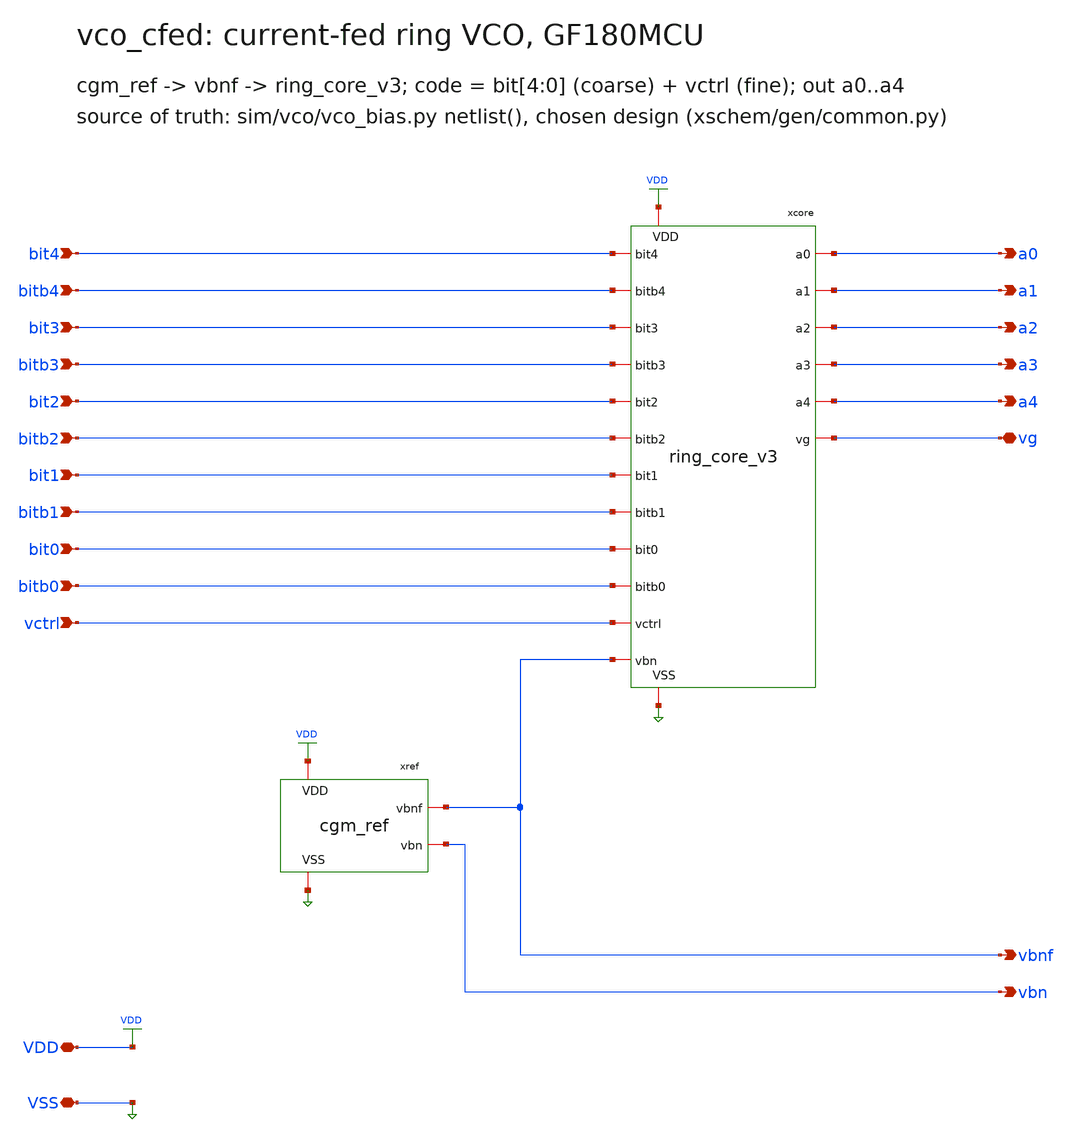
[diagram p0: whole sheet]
** sch_path: xschem/vco_cfed.sch
**.subckt vco_cfed VDD VSS vctrl bit0 bit1 bit2 bit3 bit4 bitb0 bitb1 bitb2 bitb3 bitb4 a0 a1 a2 a3
*+ a4 vg vbn vbnf
*.iopin VDD
*.iopin VSS
*.ipin vctrl
*.ipin bit0
*.ipin bit1
*.ipin bit2
*.ipin bit3
*.ipin bit4
*.ipin bitb0
*.ipin bitb1
*.ipin bitb2
*.ipin bitb3
*.ipin bitb4
*.opin a0
*.opin a1
*.opin a2
*.opin a3
*.opin a4
*.iopin vg
*.opin vbn
*.opin vbnf
xcore VDD VSS vbnf vctrl bit0 bit1 bit2 bit3 bit4 bitb0 bitb1 bitb2 bitb3 bitb4 vg a0 a1 a2 a3 a4
+ ring_core_v3
xref VDD VSS vbn vbnf cgm_ref
**.ends

* expanding   symbol:  ring_core_v3.sym # of pins=20
** sym_path: xschem/ring_core_v3.sym
** sch_path: xschem/ring_core_v3.sch
.subckt ring_core_v3 VDD VSS vbn vctrl bit0 bit1 bit2 bit3 bit4 bitb0 bitb1 bitb2 bitb3 bitb4 vg a0
+ a1 a2 a3 a4
*.iopin VDD
*.iopin VSS
*.ipin vbn
*.ipin vctrl
*.ipin bit0
*.ipin bit1
*.ipin bit2
*.ipin bit3
*.ipin bit4
*.ipin bitb0
*.ipin bitb1
*.ipin bitb2
*.ipin bitb3
*.ipin bitb4
*.iopin vg
*.opin a0
*.opin a1
*.opin a2
*.opin a3
*.opin a4
xdac vg vbn vctrl bit0 bit1 bit2 bit3 bit4 bitb0 bitb1 bitb2 bitb3 bitb4 VDD VSS cfed_dac
xring VDD vg VSS a0 a1 a2 a3 a4 cfed_ring
XDC VSS vg VSS VSS nfet_03v3 L=4.0u W=30.71u nf=1 ad=0 as=0 pd=0 ps=0 nrd=0 nrs=0 sa=0 sb=0 sd=0 m=6
.ends


* expanding   symbol:  cgm_ref.sym # of pins=4
** sym_path: xschem/cgm_ref.sym
** sch_path: xschem/cgm_ref.sch
.subckt cgm_ref VDD VSS vbn vbnf
*.iopin VDD
*.iopin VSS
*.opin vbn
*.opin vbnf
XMP2 net1 net1 VDD VDD pfet_03v3 L=14.0u W=56.0u nf=1 ad=28.0p as=28.0p pd=113.0u ps=113.0u nrd=0
+ nrs=0 sa=0 sb=0 sd=0 m=1
XMP1 vbn net1 VDD VDD pfet_03v3 L=14.0u W=56.0u nf=1 ad=28.0p as=28.0p pd=113.0u ps=113.0u nrd=0
+ nrs=0 sa=0 sb=0 sd=0 m=1
XMN2 net1 vbn net5 VSS nfet_03v3 L=1.0u W=2.0u nf=1 ad=1.0p as=1.0p pd=5.0u ps=5.0u nrd=0 nrs=0 sa=0
+ sb=0 sd=0 m=56
XMN2s1 net5 vbn net6 VSS nfet_03v3 L=1.0u W=2.0u nf=1 ad=1.0p as=1.0p pd=5.0u ps=5.0u nrd=0 nrs=0
+ sa=0 sb=0 sd=0 m=56
XMN2s2 net6 vbn net7 VSS nfet_03v3 L=1.0u W=2.0u nf=1 ad=1.0p as=1.0p pd=5.0u ps=5.0u nrd=0 nrs=0
+ sa=0 sb=0 sd=0 m=56
XMN2s3 net7 vbn net8 VSS nfet_03v3 L=1.0u W=2.0u nf=1 ad=1.0p as=1.0p pd=5.0u ps=5.0u nrd=0 nrs=0
+ sa=0 sb=0 sd=0 m=56
XMN2s4 net8 vbn net9 VSS nfet_03v3 L=1.0u W=2.0u nf=1 ad=1.0p as=1.0p pd=5.0u ps=5.0u nrd=0 nrs=0
+ sa=0 sb=0 sd=0 m=56
XMN2s5 net9 vbn net10 VSS nfet_03v3 L=1.0u W=2.0u nf=1 ad=1.0p as=1.0p pd=5.0u ps=5.0u nrd=0 nrs=0
+ sa=0 sb=0 sd=0 m=56
XMN2s6 net10 vbn net11 VSS nfet_03v3 L=1.0u W=2.0u nf=1 ad=1.0p as=1.0p pd=5.0u ps=5.0u nrd=0 nrs=0
+ sa=0 sb=0 sd=0 m=56
XMN2s7 net11 vbn net12 VSS nfet_03v3 L=1.0u W=2.0u nf=1 ad=1.0p as=1.0p pd=5.0u ps=5.0u nrd=0 nrs=0
+ sa=0 sb=0 sd=0 m=56
XMN2s8 net12 vbn net13 VSS nfet_03v3 L=1.0u W=2.0u nf=1 ad=1.0p as=1.0p pd=5.0u ps=5.0u nrd=0 nrs=0
+ sa=0 sb=0 sd=0 m=56
XMN2s9 net13 vbn net14 VSS nfet_03v3 L=1.0u W=2.0u nf=1 ad=1.0p as=1.0p pd=5.0u ps=5.0u nrd=0 nrs=0
+ sa=0 sb=0 sd=0 m=56
XMN2s10 net14 vbn net15 VSS nfet_03v3 L=1.0u W=2.0u nf=1 ad=1.0p as=1.0p pd=5.0u ps=5.0u nrd=0 nrs=0
+ sa=0 sb=0 sd=0 m=56
XMN2s11 net15 vbn net16 VSS nfet_03v3 L=1.0u W=2.0u nf=1 ad=1.0p as=1.0p pd=5.0u ps=5.0u nrd=0 nrs=0
+ sa=0 sb=0 sd=0 m=56
XMN2s12 net16 vbn net17 VSS nfet_03v3 L=1.0u W=2.0u nf=1 ad=1.0p as=1.0p pd=5.0u ps=5.0u nrd=0 nrs=0
+ sa=0 sb=0 sd=0 m=56
XMN2s13 net17 vbn net3 VSS nfet_03v3 L=1.0u W=2.0u nf=1 ad=1.0p as=1.0p pd=5.0u ps=5.0u nrd=0 nrs=0
+ sa=0 sb=0 sd=0 m=56
XMN1 vbn vbn net18 VSS nfet_03v3 L=1.0u W=2.0u nf=1 ad=1.0p as=1.0p pd=5.0u ps=5.0u nrd=0 nrs=0 sa=0
+ sb=0 sd=0 m=14
XMN1s1 net18 vbn net19 VSS nfet_03v3 L=1.0u W=2.0u nf=1 ad=1.0p as=1.0p pd=5.0u ps=5.0u nrd=0 nrs=0
+ sa=0 sb=0 sd=0 m=14
XMN1s2 net19 vbn net20 VSS nfet_03v3 L=1.0u W=2.0u nf=1 ad=1.0p as=1.0p pd=5.0u ps=5.0u nrd=0 nrs=0
+ sa=0 sb=0 sd=0 m=14
XMN1s3 net20 vbn net21 VSS nfet_03v3 L=1.0u W=2.0u nf=1 ad=1.0p as=1.0p pd=5.0u ps=5.0u nrd=0 nrs=0
+ sa=0 sb=0 sd=0 m=14
XMN1s4 net21 vbn net22 VSS nfet_03v3 L=1.0u W=2.0u nf=1 ad=1.0p as=1.0p pd=5.0u ps=5.0u nrd=0 nrs=0
+ sa=0 sb=0 sd=0 m=14
XMN1s5 net22 vbn net23 VSS nfet_03v3 L=1.0u W=2.0u nf=1 ad=1.0p as=1.0p pd=5.0u ps=5.0u nrd=0 nrs=0
+ sa=0 sb=0 sd=0 m=14
XMN1s6 net23 vbn net24 VSS nfet_03v3 L=1.0u W=2.0u nf=1 ad=1.0p as=1.0p pd=5.0u ps=5.0u nrd=0 nrs=0
+ sa=0 sb=0 sd=0 m=14
XMN1s7 net24 vbn net25 VSS nfet_03v3 L=1.0u W=2.0u nf=1 ad=1.0p as=1.0p pd=5.0u ps=5.0u nrd=0 nrs=0
+ sa=0 sb=0 sd=0 m=14
XMN1s8 net25 vbn net26 VSS nfet_03v3 L=1.0u W=2.0u nf=1 ad=1.0p as=1.0p pd=5.0u ps=5.0u nrd=0 nrs=0
+ sa=0 sb=0 sd=0 m=14
XMN1s9 net26 vbn net27 VSS nfet_03v3 L=1.0u W=2.0u nf=1 ad=1.0p as=1.0p pd=5.0u ps=5.0u nrd=0 nrs=0
+ sa=0 sb=0 sd=0 m=14
XMN1s10 net27 vbn net28 VSS nfet_03v3 L=1.0u W=2.0u nf=1 ad=1.0p as=1.0p pd=5.0u ps=5.0u nrd=0 nrs=0
+ sa=0 sb=0 sd=0 m=14
XMN1s11 net28 vbn net29 VSS nfet_03v3 L=1.0u W=2.0u nf=1 ad=1.0p as=1.0p pd=5.0u ps=5.0u nrd=0 nrs=0
+ sa=0 sb=0 sd=0 m=14
XMN1s12 net29 vbn net30 VSS nfet_03v3 L=1.0u W=2.0u nf=1 ad=1.0p as=1.0p pd=5.0u ps=5.0u nrd=0 nrs=0
+ sa=0 sb=0 sd=0 m=14
XMN1s13 net30 vbn VSS VSS nfet_03v3 L=1.0u W=2.0u nf=1 ad=1.0p as=1.0p pd=5.0u ps=5.0u nrd=0 nrs=0
+ sa=0 sb=0 sd=0 m=14
XMS1 net2 VSS VDD VDD pfet_03v3 L=10.0u W=0.5u nf=1 ad=0.25p as=0.25p pd=2.0u ps=2.0u nrd=0 nrs=0
+ sa=0 sb=0 sd=0 m=1
XMS2 net2 vbn VSS VSS nfet_03v3 L=0.28u W=2.0u nf=1 ad=1.0p as=1.0p pd=5.0u ps=5.0u nrd=0 nrs=0 sa=0
+ sb=0 sd=0 m=1
XMS3 net1 net2 vbn VSS nfet_03v3 L=0.28u W=1.0u nf=1 ad=0.5p as=0.5p pd=3.0u ps=3.0u nrd=0 nrs=0
+ sa=0 sb=0 sd=0 m=1
XRBW net3 net4 VSS nwell r_width=2.0e-6 r_length=5.023e-6 m=1
XRBN net4 VSS VSS nplus_u r_width=2.0e-6 r_length=100.0e-6 m=1
XRF vbn vbnf VSS ppolyf_u_3k r_width=1.0e-6 r_length=318.271e-6 m=1
CF vbnf VSS 2e-11 m=1
.ends


* expanding   symbol:  cfed_dac.sym # of pins=15
** sym_path: xschem/cfed_dac.sym
** sch_path: xschem/cfed_dac.sch
.subckt cfed_dac vg vbnf vctrl bit0 bit1 bit2 bit3 bit4 bitb0 bitb1 bitb2 bitb3 bitb4 VDD VSS
*.iopin vg
*.ipin vbnf
*.ipin vctrl
*.ipin bit0
*.ipin bit1
*.ipin bit2
*.ipin bit3
*.ipin bit4
*.ipin bitb0
*.ipin bitb1
*.ipin bitb2
*.ipin bitb3
*.ipin bitb4
*.iopin VDD
*.iopin VSS
XFFC vg vctrl VSS VSS nfet_03v3 L=21.333333333333332u W=1.2u nf=1 ad=0.6p as=0.6p pd=3.4u ps=3.4u
+ nrd=0 nrs=0 sa=0 sb=0 sd=0 m=1
XFC vg vbnf VSS VSS nfet_03v3 L=5.333333333333333u W=1.2u nf=1 ad=0.6p as=0.6p pd=3.4u ps=3.4u nrd=0
+ nrs=0 sa=0 sb=0 sd=0 m=6
XFC_0 vg net1 VSS VSS nfet_03v3 L=5.333333333333333u W=1.2u nf=1 ad=0.6p as=0.6p pd=3.4u ps=3.4u
+ nrd=0 nrs=0 sa=0 sb=0 sd=0 m=1
XFC_1 vg net2 VSS VSS nfet_03v3 L=5.333333333333333u W=1.2u nf=1 ad=0.6p as=0.6p pd=3.4u ps=3.4u
+ nrd=0 nrs=0 sa=0 sb=0 sd=0 m=2
XFC_2 vg net3 VSS VSS nfet_03v3 L=5.333333333333333u W=1.2u nf=1 ad=0.6p as=0.6p pd=3.4u ps=3.4u
+ nrd=0 nrs=0 sa=0 sb=0 sd=0 m=4
XFC_3 vg net4 VSS VSS nfet_03v3 L=5.333333333333333u W=1.2u nf=1 ad=0.6p as=0.6p pd=3.4u ps=3.4u
+ nrd=0 nrs=0 sa=0 sb=0 sd=0 m=8
XFC_4 vg net5 VSS VSS nfet_03v3 L=5.333333333333333u W=1.2u nf=1 ad=0.6p as=0.6p pd=3.4u ps=3.4u
+ nrd=0 nrs=0 sa=0 sb=0 sd=0 m=16
XTP0 net1 bitb0 vbnf VDD pfet_03v3 L=0.28u W=5.0u nf=1 ad=2.5p as=2.5p pd=11.0u ps=11.0u nrd=0 nrs=0
+ sa=0 sb=0 sd=0 m=1
XTN0 net1 bit0 vbnf VSS nfet_03v3 L=0.28u W=2.0u nf=1 ad=1.0p as=1.0p pd=5.0u ps=5.0u nrd=0 nrs=0
+ sa=0 sb=0 sd=0 m=1
XTD0 net1 bitb0 VSS VSS nfet_03v3 L=0.28u W=1.0u nf=1 ad=0.5p as=0.5p pd=3.0u ps=3.0u nrd=0 nrs=0
+ sa=0 sb=0 sd=0 m=1
XTP1 net2 bitb1 vbnf VDD pfet_03v3 L=0.28u W=5.0u nf=1 ad=2.5p as=2.5p pd=11.0u ps=11.0u nrd=0 nrs=0
+ sa=0 sb=0 sd=0 m=1
XTN1 net2 bit1 vbnf VSS nfet_03v3 L=0.28u W=2.0u nf=1 ad=1.0p as=1.0p pd=5.0u ps=5.0u nrd=0 nrs=0
+ sa=0 sb=0 sd=0 m=1
XTD1 net2 bitb1 VSS VSS nfet_03v3 L=0.28u W=1.0u nf=1 ad=0.5p as=0.5p pd=3.0u ps=3.0u nrd=0 nrs=0
+ sa=0 sb=0 sd=0 m=1
XTP2 net3 bitb2 vbnf VDD pfet_03v3 L=0.28u W=5.0u nf=1 ad=2.5p as=2.5p pd=11.0u ps=11.0u nrd=0 nrs=0
+ sa=0 sb=0 sd=0 m=1
XTN2 net3 bit2 vbnf VSS nfet_03v3 L=0.28u W=2.0u nf=1 ad=1.0p as=1.0p pd=5.0u ps=5.0u nrd=0 nrs=0
+ sa=0 sb=0 sd=0 m=1
XTD2 net3 bitb2 VSS VSS nfet_03v3 L=0.28u W=1.0u nf=1 ad=0.5p as=0.5p pd=3.0u ps=3.0u nrd=0 nrs=0
+ sa=0 sb=0 sd=0 m=1
XTP3 net4 bitb3 vbnf VDD pfet_03v3 L=0.28u W=5.0u nf=1 ad=2.5p as=2.5p pd=11.0u ps=11.0u nrd=0 nrs=0
+ sa=0 sb=0 sd=0 m=1
XTN3 net4 bit3 vbnf VSS nfet_03v3 L=0.28u W=2.0u nf=1 ad=1.0p as=1.0p pd=5.0u ps=5.0u nrd=0 nrs=0
+ sa=0 sb=0 sd=0 m=1
XTD3 net4 bitb3 VSS VSS nfet_03v3 L=0.28u W=1.0u nf=1 ad=0.5p as=0.5p pd=3.0u ps=3.0u nrd=0 nrs=0
+ sa=0 sb=0 sd=0 m=1
XTP4 net5 bitb4 vbnf VDD pfet_03v3 L=0.28u W=5.0u nf=1 ad=2.5p as=2.5p pd=11.0u ps=11.0u nrd=0 nrs=0
+ sa=0 sb=0 sd=0 m=1
XTN4 net5 bit4 vbnf VSS nfet_03v3 L=0.28u W=2.0u nf=1 ad=1.0p as=1.0p pd=5.0u ps=5.0u nrd=0 nrs=0
+ sa=0 sb=0 sd=0 m=1
XTD4 net5 bitb4 VSS VSS nfet_03v3 L=0.28u W=1.0u nf=1 ad=0.5p as=0.5p pd=3.0u ps=3.0u nrd=0 nrs=0
+ sa=0 sb=0 sd=0 m=1
.ends


* expanding   symbol:  cfed_ring.sym # of pins=8
** sym_path: xschem/cfed_ring.sym
** sch_path: xschem/cfed_ring.sch
.subckt cfed_ring VDD vg VSS a0 a1 a2 a3 a4
*.iopin VDD
*.iopin vg
*.iopin VSS
*.opin a0
*.opin a1
*.opin a2
*.opin a3
*.opin a4
XP0 a1 a0 VDD VDD pfet_03v3 L=0.28u W=5.0u nf=1 ad=2.5p as=2.5p pd=11.0u ps=11.0u nrd=0 nrs=0 sa=0
+ sb=0 sd=0 m=1
XN0 a1 a0 vg VSS nfet_03v3 L=0.28u W=2.0u nf=1 ad=1.0p as=1.0p pd=5.0u ps=5.0u nrd=0 nrs=0 sa=0 sb=0
+ sd=0 m=1
XP1 a2 a1 VDD VDD pfet_03v3 L=0.28u W=5.0u nf=1 ad=2.5p as=2.5p pd=11.0u ps=11.0u nrd=0 nrs=0 sa=0
+ sb=0 sd=0 m=1
XN1 a2 a1 vg VSS nfet_03v3 L=0.28u W=2.0u nf=1 ad=1.0p as=1.0p pd=5.0u ps=5.0u nrd=0 nrs=0 sa=0 sb=0
+ sd=0 m=1
XP2 a3 a2 VDD VDD pfet_03v3 L=0.28u W=5.0u nf=1 ad=2.5p as=2.5p pd=11.0u ps=11.0u nrd=0 nrs=0 sa=0
+ sb=0 sd=0 m=1
XN2 a3 a2 vg VSS nfet_03v3 L=0.28u W=2.0u nf=1 ad=1.0p as=1.0p pd=5.0u ps=5.0u nrd=0 nrs=0 sa=0 sb=0
+ sd=0 m=1
XP3 a4 a3 VDD VDD pfet_03v3 L=0.28u W=5.0u nf=1 ad=2.5p as=2.5p pd=11.0u ps=11.0u nrd=0 nrs=0 sa=0
+ sb=0 sd=0 m=1
XN3 a4 a3 vg VSS nfet_03v3 L=0.28u W=2.0u nf=1 ad=1.0p as=1.0p pd=5.0u ps=5.0u nrd=0 nrs=0 sa=0 sb=0
+ sd=0 m=1
XP4 a0 a4 VDD VDD pfet_03v3 L=0.28u W=5.0u nf=1 ad=2.5p as=2.5p pd=11.0u ps=11.0u nrd=0 nrs=0 sa=0
+ sb=0 sd=0 m=1
XN4 a0 a4 vg VSS nfet_03v3 L=0.28u W=2.0u nf=1 ad=1.0p as=1.0p pd=5.0u ps=5.0u nrd=0 nrs=0 sa=0 sb=0
+ sd=0 m=1
.ends

.end
